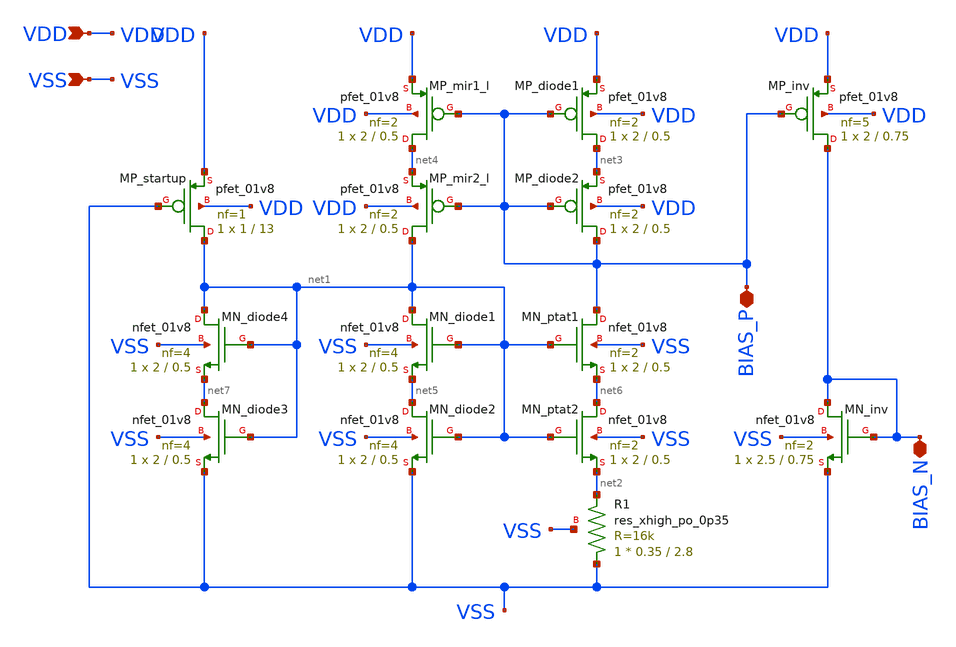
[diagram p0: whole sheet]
** sch_path: schem/symbol_repo/sym_ptat.sch
**.subckt sym_ptat VDD VSS BIAS_P BIAS_N
*.ipin VDD
*.ipin VSS
*.iopin BIAS_P
*.iopin BIAS_N
XMN_ptat2 net6 net1 net2 VSS sky130_fd_pr__nfet_01v8 L=0.5 W=2 nf=2 ad='int((2 + 1)/2) * 2 / 2 * 0.29'
+ as='int((2 + 2)/2) * 2 / 2 * 0.29' pd='2*int((2 + 1)/2) * (2 / 2 + 0.29)' ps='2*int((2 + 2)/2) * (2 / 2 + 0.29)'
+ nrd='0.29 / 2 ' nrs='0.29 / 2 ' sa=0 sb=0 sd=0 mult=1 m=1
XMP_diode1 net3 BIAS_P VDD VDD sky130_fd_pr__pfet_01v8 L=0.5 W=2 nf=2 ad='int((2 + 1)/2) * 2 / 2 * 0.29'
+ as='int((2 + 2)/2) * 2 / 2 * 0.29' pd='2*int((2 + 1)/2) * (2 / 2 + 0.29)' ps='2*int((2 + 2)/2) * (2 / 2 + 0.29)'
+ nrd='0.29 / 2 ' nrs='0.29 / 2 ' sa=0 sb=0 sd=0 mult=1 m=1
XMP_mir1_l net4 BIAS_P VDD VDD sky130_fd_pr__pfet_01v8 L=0.5 W=2 nf=2 ad='int((2 + 1)/2) * 2 / 2 * 0.29'
+ as='int((2 + 2)/2) * 2 / 2 * 0.29' pd='2*int((2 + 1)/2) * (2 / 2 + 0.29)' ps='2*int((2 + 2)/2) * (2 / 2 + 0.29)'
+ nrd='0.29 / 2 ' nrs='0.29 / 2 ' sa=0 sb=0 sd=0 mult=1 m=1
XMN_diode2 net5 net1 VSS VSS sky130_fd_pr__nfet_01v8 L=0.5 W=2 nf=4 ad='int((4 + 1)/2) * 2 / 4 * 0.29'
+ as='int((4 + 2)/2) * 2 / 4 * 0.29' pd='2*int((4 + 1)/2) * (2 / 4 + 0.29)' ps='2*int((4 + 2)/2) * (2 / 4 + 0.29)'
+ nrd='0.29 / 2 ' nrs='0.29 / 2 ' sa=0 sb=0 sd=0 mult=1 m=1
XMP_inv BIAS_N BIAS_P VDD VDD sky130_fd_pr__pfet_01v8 L=0.75 W=2 nf=5 ad='int((5 + 1)/2) * 2 / 5 * 0.29'
+ as='int((5 + 2)/2) * 2 / 5 * 0.29' pd='2*int((5 + 1)/2) * (2 / 5 + 0.29)' ps='2*int((5 + 2)/2) * (2 / 5 + 0.29)'
+ nrd='0.29 / 2 ' nrs='0.29 / 2 ' sa=0 sb=0 sd=0 mult=1 m=1
XMP_diode2 BIAS_P BIAS_P net3 VDD sky130_fd_pr__pfet_01v8 L=0.5 W=2 nf=2 ad='int((2 + 1)/2) * 2 / 2 * 0.29'
+ as='int((2 + 2)/2) * 2 / 2 * 0.29' pd='2*int((2 + 1)/2) * (2 / 2 + 0.29)' ps='2*int((2 + 2)/2) * (2 / 2 + 0.29)'
+ nrd='0.29 / 2 ' nrs='0.29 / 2 ' sa=0 sb=0 sd=0 mult=1 m=1
XMP_mir2_l net1 BIAS_P net4 VDD sky130_fd_pr__pfet_01v8 L=0.5 W=2 nf=2 ad='int((2 + 1)/2) * 2 / 2 * 0.29'
+ as='int((2 + 2)/2) * 2 / 2 * 0.29' pd='2*int((2 + 1)/2) * (2 / 2 + 0.29)' ps='2*int((2 + 2)/2) * (2 / 2 + 0.29)'
+ nrd='0.29 / 2 ' nrs='0.29 / 2 ' sa=0 sb=0 sd=0 mult=1 m=1
XMN_ptat1 BIAS_P net1 net6 VSS sky130_fd_pr__nfet_01v8 L=0.5 W=2 nf=2 ad='int((2 + 1)/2) * 2 / 2 * 0.29'
+ as='int((2 + 2)/2) * 2 / 2 * 0.29' pd='2*int((2 + 1)/2) * (2 / 2 + 0.29)' ps='2*int((2 + 2)/2) * (2 / 2 + 0.29)'
+ nrd='0.29 / 2 ' nrs='0.29 / 2 ' sa=0 sb=0 sd=0 mult=1 m=1
XMN_diode1 net1 net1 net5 VSS sky130_fd_pr__nfet_01v8 L=0.5 W=2 nf=4 ad='int((4 + 1)/2) * 2 / 4 * 0.29'
+ as='int((4 + 2)/2) * 2 / 4 * 0.29' pd='2*int((4 + 1)/2) * (2 / 4 + 0.29)' ps='2*int((4 + 2)/2) * (2 / 4 + 0.29)'
+ nrd='0.29 / 2 ' nrs='0.29 / 2 ' sa=0 sb=0 sd=0 mult=1 m=1
XMN_inv BIAS_N BIAS_N VSS VSS sky130_fd_pr__nfet_01v8 L=0.75 W=2.5 nf=2 ad='int((2 + 1)/2) * 2.5 / 2 * 0.29'
+ as='int((2 + 2)/2) * 2.5 / 2 * 0.29' pd='2*int((2 + 1)/2) * (2.5 / 2 + 0.29)' ps='2*int((2 + 2)/2) * (2.5 / 2 + 0.29)'
+ nrd='0.29 / 2.5 ' nrs='0.29 / 2.5 ' sa=0 sb=0 sd=0 mult=1 m=1
XR1 VSS net2 VSS sky130_fd_pr__res_xhigh_po_0p35 L=2.8 mult=1 m=1
XMP_startup net1 VSS VDD VDD sky130_fd_pr__pfet_01v8 L=13 W=1 nf=1 ad='int((1 + 1)/2) * 1 / 1 * 0.29'
+ as='int((1 + 2)/2) * 1 / 1 * 0.29' pd='2*int((1 + 1)/2) * (1 / 1 + 0.29)' ps='2*int((1 + 2)/2) * (1 / 1 + 0.29)'
+ nrd='0.29 / 1 ' nrs='0.29 / 1 ' sa=0 sb=0 sd=0 mult=1 m=1
XMN_diode3 net7 net1 VSS VSS sky130_fd_pr__nfet_01v8 L=0.5 W=2 nf=4 ad='int((4 + 1)/2) * 2 / 4 * 0.29'
+ as='int((4 + 2)/2) * 2 / 4 * 0.29' pd='2*int((4 + 1)/2) * (2 / 4 + 0.29)' ps='2*int((4 + 2)/2) * (2 / 4 + 0.29)'
+ nrd='0.29 / 2 ' nrs='0.29 / 2 ' sa=0 sb=0 sd=0 mult=1 m=1
XMN_diode4 net1 net1 net7 VSS sky130_fd_pr__nfet_01v8 L=0.5 W=2 nf=4 ad='int((4 + 1)/2) * 2 / 4 * 0.29'
+ as='int((4 + 2)/2) * 2 / 4 * 0.29' pd='2*int((4 + 1)/2) * (2 / 4 + 0.29)' ps='2*int((4 + 2)/2) * (2 / 4 + 0.29)'
+ nrd='0.29 / 2 ' nrs='0.29 / 2 ' sa=0 sb=0 sd=0 mult=1 m=1
**.ends
.end
